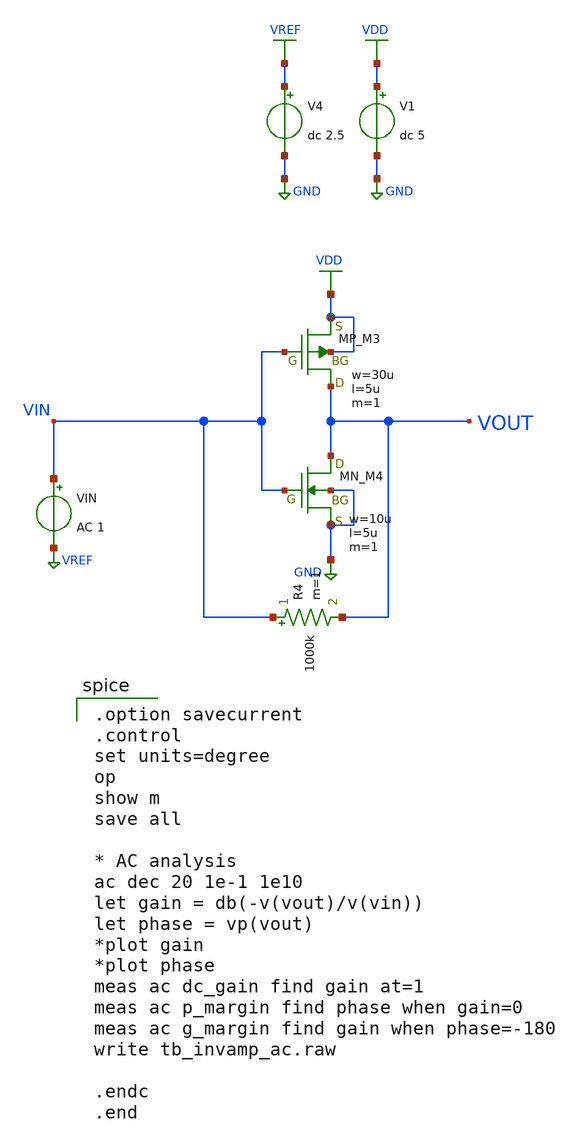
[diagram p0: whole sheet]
** sch_path: member_project/AM_Radio/Yamada3/xschem/tb_invamp_ac.sch
**.subckt tb_invamp_ac
VIN VIN VREF AC 1
V1 VDD GND dc 5
V4 VREF GND dc 2.5
XM3 VOUT VIN VDD VDD PMOS w=30u l=5u as=0 ad=0 ps=0 pd=0 nrd=0 nrs=0 m=1
XM4 VOUT VIN GND GND NMOS w=10u l=5u as=0 ad=0 ps=0 pd=0 nrd=0 nrs=0 m=1
R4 VIN VOUT 1000k m=1
**** begin user architecture code

.option savecurrent
.control
set units=degree
op
show m
save all

* AC analysis
ac dec 20 1e-1 1e10
let gain = db(-v(vout)/v(vin))
let phase = vp(vout)
*plot gain
*plot phase
meas ac dc_gain find gain at=1
meas ac p_margin find phase when gain=0
meas ac g_margin find gain when phase=-180
write tb_invamp_ac.raw

.endc
.end


 .include $::LIB/ip62_models
**** end user architecture code
**.ends
.GLOBAL VREF
.GLOBAL VDD
.GLOBAL GND
.end
